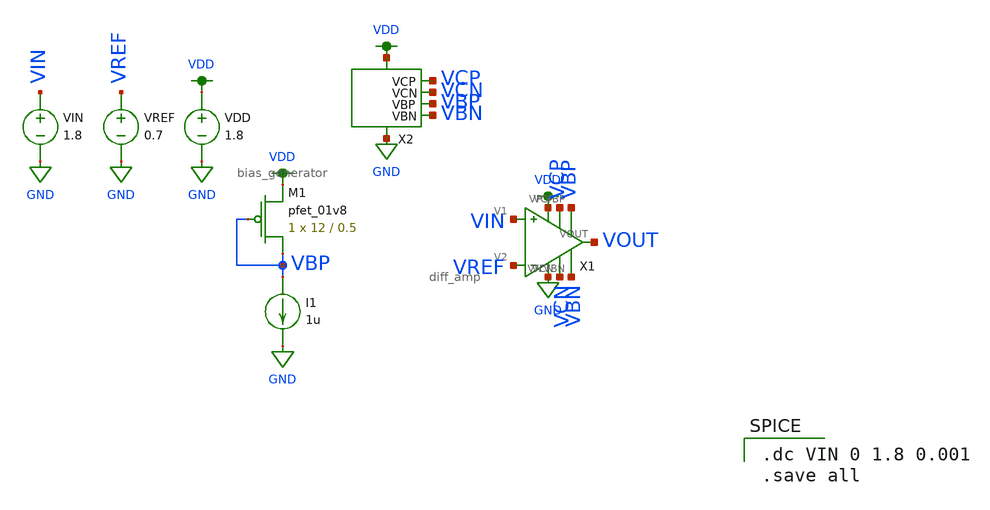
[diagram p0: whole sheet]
** sch_path: mp3/schematics/bias_generator_tran.sch
**.subckt bias_generator_tran
VDD VDD GND 1.8
I1 VBP GND 1u
VREF VREF GND 0.7
VIN VIN GND 1.8
XM1 VBP VBP VDD VDD sky130_fd_pr__pfet_01v8 L=0.5 W=12 nf=1 ad='int((nf+1)/2) * W/nf * 0.29' as='int((nf+2)/2) * W/nf * 0.29'
+ pd='2*int((nf+1)/2) * (W/nf + 0.29)' ps='2*int((nf+2)/2) * (W/nf + 0.29)' nrd='0.29 / W' nrs='0.29 / W'
+ sa=0 sb=0 sd=0 mult=1 m=1
X1 VIN VREF VDD GND VCN VBN VBP VCP VOUT diff_amp
X2 VDD GND VCN VCP VBP VBN bias_generator
**** begin user architecture code

.option wnflag=1
.lib ~/skywater/skywater-pdk/libraries/sky130_fd_pr_ngspice/latest/models/sky130.lib.spice tt


.dc VIN 0 1.8 0.001
.save all

**** end user architecture code
**.ends

* expanding   symbol:  /home/madvlsi/Documents/VLSI/mp3/schematics/diff_amp.sym # of pins=9
** sym_path: mp3/schematics/diff_amp.sym
** sch_path: mp3/schematics/diff_amp.sch
.subckt diff_amp V1 V2 VP VN VCN VBN VBP VCP VOUT
*.ipin V1
*.ipin V2
*.iopin VP
*.iopin VN
*.opin VOUT
*.iopin VBP
*.iopin VCP
*.iopin VCN
*.iopin VBN
XM1 net1 VBP VP VP sky130_fd_pr__pfet_01v8 L=0.5 W=12 nf=1 ad='int((nf+1)/2) * W/nf * 0.29' as='int((nf+2)/2) * W/nf * 0.29'
+ pd='2*int((nf+1)/2) * (W/nf + 0.29)' ps='2*int((nf+2)/2) * (W/nf + 0.29)' nrd='0.29 / W' nrs='0.29 / W'
+ sa=0 sb=0 sd=0 mult=1 m=1
XM5 net3 VCN net4 VN sky130_fd_pr__nfet_01v8 L=0.5 W=12 nf=1 ad='int((nf+1)/2) * W/nf * 0.29' as='int((nf+2)/2) * W/nf * 0.29'
+ pd='2*int((nf+1)/2) * (W/nf + 0.29)' ps='2*int((nf+2)/2) * (W/nf + 0.29)' nrd='0.29 / W' nrs='0.29 / W'
+ sa=0 sb=0 sd=0 mult=1 m=1
XM2 net2 VBP VP VP sky130_fd_pr__pfet_01v8 L=0.5 W=12 nf=1 ad='int((nf+1)/2) * W/nf * 0.29' as='int((nf+2)/2) * W/nf * 0.29'
+ pd='2*int((nf+1)/2) * (W/nf + 0.29)' ps='2*int((nf+2)/2) * (W/nf + 0.29)' nrd='0.29 / W' nrs='0.29 / W'
+ sa=0 sb=0 sd=0 mult=1 m=1
XM3 VOUT VCP net2 VP sky130_fd_pr__pfet_01v8 L=0.5 W=12 nf=1 ad='int((nf+1)/2) * W/nf * 0.29' as='int((nf+2)/2) * W/nf * 0.29'
+ pd='2*int((nf+1)/2) * (W/nf + 0.29)' ps='2*int((nf+2)/2) * (W/nf + 0.29)' nrd='0.29 / W' nrs='0.29 / W'
+ sa=0 sb=0 sd=0 mult=1 m=1
XM4 net3 VCP net1 VP sky130_fd_pr__pfet_01v8 L=0.5 W=12 nf=1 ad='int((nf+1)/2) * W/nf * 0.29' as='int((nf+2)/2) * W/nf * 0.29'
+ pd='2*int((nf+1)/2) * (W/nf + 0.29)' ps='2*int((nf+2)/2) * (W/nf + 0.29)' nrd='0.29 / W' nrs='0.29 / W'
+ sa=0 sb=0 sd=0 mult=1 m=1
XM6 net1 V1 net6 VN sky130_fd_pr__nfet_01v8 L=0.5 W=12 nf=1 ad='int((nf+1)/2) * W/nf * 0.29' as='int((nf+2)/2) * W/nf * 0.29'
+ pd='2*int((nf+1)/2) * (W/nf + 0.29)' ps='2*int((nf+2)/2) * (W/nf + 0.29)' nrd='0.29 / W' nrs='0.29 / W'
+ sa=0 sb=0 sd=0 mult=1 m=1
XM7 net2 V2 net6 VN sky130_fd_pr__nfet_01v8 L=0.5 W=12 nf=1 ad='int((nf+1)/2) * W/nf * 0.29' as='int((nf+2)/2) * W/nf * 0.29'
+ pd='2*int((nf+1)/2) * (W/nf + 0.29)' ps='2*int((nf+2)/2) * (W/nf + 0.29)' nrd='0.29 / W' nrs='0.29 / W'
+ sa=0 sb=0 sd=0 mult=1 m=1
XM8 VOUT VCN net5 VN sky130_fd_pr__nfet_01v8 L=0.5 W=12 nf=1 ad='int((nf+1)/2) * W/nf * 0.29' as='int((nf+2)/2) * W/nf * 0.29'
+ pd='2*int((nf+1)/2) * (W/nf + 0.29)' ps='2*int((nf+2)/2) * (W/nf + 0.29)' nrd='0.29 / W' nrs='0.29 / W'
+ sa=0 sb=0 sd=0 mult=1 m=1
XM9 net5 net3 VN VN sky130_fd_pr__nfet_01v8 L=0.5 W=12 nf=1 ad='int((nf+1)/2) * W/nf * 0.29' as='int((nf+2)/2) * W/nf * 0.29'
+ pd='2*int((nf+1)/2) * (W/nf + 0.29)' ps='2*int((nf+2)/2) * (W/nf + 0.29)' nrd='0.29 / W' nrs='0.29 / W'
+ sa=0 sb=0 sd=0 mult=1 m=1
XM10 net4 net3 VN VN sky130_fd_pr__nfet_01v8 L=0.5 W=12 nf=1 ad='int((nf+1)/2) * W/nf * 0.29' as='int((nf+2)/2) * W/nf * 0.29'
+ pd='2*int((nf+1)/2) * (W/nf + 0.29)' ps='2*int((nf+2)/2) * (W/nf + 0.29)' nrd='0.29 / W' nrs='0.29 / W'
+ sa=0 sb=0 sd=0 mult=1 m=1
XM11 net6 VBN VN VN sky130_fd_pr__nfet_01v8 L=0.5 W=12 nf=1 ad='int((nf+1)/2) * W/nf * 0.29' as='int((nf+2)/2) * W/nf * 0.29'
+ pd='2*int((nf+1)/2) * (W/nf + 0.29)' ps='2*int((nf+2)/2) * (W/nf + 0.29)' nrd='0.29 / W' nrs='0.29 / W'
+ sa=0 sb=0 sd=0 mult=1 m=1
.ends


* expanding   symbol:  /home/madvlsi/Documents/VLSI/mp3/schematics/bias_generator.sym # of pins=6
** sym_path: mp3/schematics/bias_generator.sym
** sch_path: mp3/schematics/bias_generator.sch
.subckt bias_generator VP VN VCN VCP VBP VBN
*.iopin VBP
*.iopin VP
*.iopin VN
*.opin VCN
*.opin VCP
*.opin VBN
XM9 VCN VP VP VP sky130_fd_pr__pfet_01v8 L=0.5 W=12 nf=1 ad='int((nf+1)/2) * W/nf * 0.29' as='int((nf+2)/2) * W/nf * 0.29'
+ pd='2*int((nf+1)/2) * (W/nf + 0.29)' ps='2*int((nf+2)/2) * (W/nf + 0.29)' nrd='0.29 / W' nrs='0.29 / W'
+ sa=0 sb=0 sd=0 mult=1 m=1
XM24 VCN VCN net10 GND sky130_fd_pr__nfet_01v8 L=0.5 W=12 nf=1 ad='int((nf+1)/2) * W/nf * 0.29' as='int((nf+2)/2) * W/nf * 0.29'
+ pd='2*int((nf+1)/2) * (W/nf + 0.29)' ps='2*int((nf+2)/2) * (W/nf + 0.29)' nrd='0.29 / W' nrs='0.29 / W'
+ sa=0 sb=0 sd=0 mult=1 m=1
XM2 VCN VBP VP VDD sky130_fd_pr__pfet_01v8 L=0.5 W=12 nf=1 ad='int((nf+1)/2) * W/nf * 0.29' as='int((nf+2)/2) * W/nf * 0.29'
+ pd='2*int((nf+1)/2) * (W/nf + 0.29)' ps='2*int((nf+2)/2) * (W/nf + 0.29)' nrd='0.29 / W' nrs='0.29 / W'
+ sa=0 sb=0 sd=0 mult=1 m=1
XM1 VP VBP net1 VDD sky130_fd_pr__pfet_01v8 L=0.5 W=12 nf=1 ad='int((nf+1)/2) * W/nf * 0.29' as='int((nf+2)/2) * W/nf * 0.29'
+ pd='2*int((nf+1)/2) * (W/nf + 0.29)' ps='2*int((nf+2)/2) * (W/nf + 0.29)' nrd='0.29 / W' nrs='0.29 / W'
+ sa=0 sb=0 sd=0 mult=1 m=1
XM3 net1 VBP net2 VDD sky130_fd_pr__pfet_01v8 L=0.5 W=12 nf=1 ad='int((nf+1)/2) * W/nf * 0.29' as='int((nf+2)/2) * W/nf * 0.29'
+ pd='2*int((nf+1)/2) * (W/nf + 0.29)' ps='2*int((nf+2)/2) * (W/nf + 0.29)' nrd='0.29 / W' nrs='0.29 / W'
+ sa=0 sb=0 sd=0 mult=1 m=1
XM4 net2 VBP net3 VDD sky130_fd_pr__pfet_01v8 L=0.5 W=12 nf=1 ad='int((nf+1)/2) * W/nf * 0.29' as='int((nf+2)/2) * W/nf * 0.29'
+ pd='2*int((nf+1)/2) * (W/nf + 0.29)' ps='2*int((nf+2)/2) * (W/nf + 0.29)' nrd='0.29 / W' nrs='0.29 / W'
+ sa=0 sb=0 sd=0 mult=1 m=1
XM6 net3 VBP net4 VDD sky130_fd_pr__pfet_01v8 L=0.5 W=12 nf=1 ad='int((nf+1)/2) * W/nf * 0.29' as='int((nf+2)/2) * W/nf * 0.29'
+ pd='2*int((nf+1)/2) * (W/nf + 0.29)' ps='2*int((nf+2)/2) * (W/nf + 0.29)' nrd='0.29 / W' nrs='0.29 / W'
+ sa=0 sb=0 sd=0 mult=1 m=1
XM7 net4 VBP net9 VDD sky130_fd_pr__pfet_01v8 L=0.5 W=12 nf=1 ad='int((nf+1)/2) * W/nf * 0.29' as='int((nf+2)/2) * W/nf * 0.29'
+ pd='2*int((nf+1)/2) * (W/nf + 0.29)' ps='2*int((nf+2)/2) * (W/nf + 0.29)' nrd='0.29 / W' nrs='0.29 / W'
+ sa=0 sb=0 sd=0 mult=1 m=1
XM8 net9 VBP net5 VDD sky130_fd_pr__pfet_01v8 L=0.5 W=12 nf=1 ad='int((nf+1)/2) * W/nf * 0.29' as='int((nf+2)/2) * W/nf * 0.29'
+ pd='2*int((nf+1)/2) * (W/nf + 0.29)' ps='2*int((nf+2)/2) * (W/nf + 0.29)' nrd='0.29 / W' nrs='0.29 / W'
+ sa=0 sb=0 sd=0 mult=1 m=1
XM52 net5 VBP net6 VDD sky130_fd_pr__pfet_01v8 L=0.5 W=12 nf=1 ad='int((nf+1)/2) * W/nf * 0.29' as='int((nf+2)/2) * W/nf * 0.29'
+ pd='2*int((nf+1)/2) * (W/nf + 0.29)' ps='2*int((nf+2)/2) * (W/nf + 0.29)' nrd='0.29 / W' nrs='0.29 / W'
+ sa=0 sb=0 sd=0 mult=1 m=1
XM53 net6 VBP net7 VDD sky130_fd_pr__pfet_01v8 L=0.5 W=12 nf=1 ad='int((nf+1)/2) * W/nf * 0.29' as='int((nf+2)/2) * W/nf * 0.29'
+ pd='2*int((nf+1)/2) * (W/nf + 0.29)' ps='2*int((nf+2)/2) * (W/nf + 0.29)' nrd='0.29 / W' nrs='0.29 / W'
+ sa=0 sb=0 sd=0 mult=1 m=1
XM54 net7 VBP net8 VDD sky130_fd_pr__pfet_01v8 L=0.5 W=12 nf=1 ad='int((nf+1)/2) * W/nf * 0.29' as='int((nf+2)/2) * W/nf * 0.29'
+ pd='2*int((nf+1)/2) * (W/nf + 0.29)' ps='2*int((nf+2)/2) * (W/nf + 0.29)' nrd='0.29 / W' nrs='0.29 / W'
+ sa=0 sb=0 sd=0 mult=1 m=1
XM55 net8 VBP VP VDD sky130_fd_pr__pfet_01v8 L=0.5 W=12 nf=1 ad='int((nf+1)/2) * W/nf * 0.29' as='int((nf+2)/2) * W/nf * 0.29'
+ pd='2*int((nf+1)/2) * (W/nf + 0.29)' ps='2*int((nf+2)/2) * (W/nf + 0.29)' nrd='0.29 / W' nrs='0.29 / W'
+ sa=0 sb=0 sd=0 mult=1 m=1
XM56 VP VBP VCN VDD sky130_fd_pr__pfet_01v8 L=0.5 W=12 nf=1 ad='int((nf+1)/2) * W/nf * 0.29' as='int((nf+2)/2) * W/nf * 0.29'
+ pd='2*int((nf+1)/2) * (W/nf + 0.29)' ps='2*int((nf+2)/2) * (W/nf + 0.29)' nrd='0.29 / W' nrs='0.29 / W'
+ sa=0 sb=0 sd=0 mult=1 m=1
XM10 VP VP VCN VP sky130_fd_pr__pfet_01v8 L=0.5 W=12 nf=1 ad='int((nf+1)/2) * W/nf * 0.29' as='int((nf+2)/2) * W/nf * 0.29'
+ pd='2*int((nf+1)/2) * (W/nf + 0.29)' ps='2*int((nf+2)/2) * (W/nf + 0.29)' nrd='0.29 / W' nrs='0.29 / W'
+ sa=0 sb=0 sd=0 mult=1 m=1
XM25 VN VN VCN VN sky130_fd_pr__nfet_01v8 L=0.5 W=12 nf=1 ad='int((nf+1)/2) * W/nf * 0.29' as='int((nf+2)/2) * W/nf * 0.29'
+ pd='2*int((nf+1)/2) * (W/nf + 0.29)' ps='2*int((nf+2)/2) * (W/nf + 0.29)' nrd='0.29 / W' nrs='0.29 / W'
+ sa=0 sb=0 sd=0 mult=1 m=1
XM14 net9 net9 net10 GND sky130_fd_pr__nfet_01v8 L=0.5 W=12 nf=1 ad='int((nf+1)/2) * W/nf * 0.29' as='int((nf+2)/2) * W/nf * 0.29'
+ pd='2*int((nf+1)/2) * (W/nf + 0.29)' ps='2*int((nf+2)/2) * (W/nf + 0.29)' nrd='0.29 / W' nrs='0.29 / W'
+ sa=0 sb=0 sd=0 mult=1 m=1
XM15 net10 net9 net9 GND sky130_fd_pr__nfet_01v8 L=0.5 W=12 nf=1 ad='int((nf+1)/2) * W/nf * 0.29' as='int((nf+2)/2) * W/nf * 0.29'
+ pd='2*int((nf+1)/2) * (W/nf + 0.29)' ps='2*int((nf+2)/2) * (W/nf + 0.29)' nrd='0.29 / W' nrs='0.29 / W'
+ sa=0 sb=0 sd=0 mult=1 m=1
XM16 net9 net9 net10 GND sky130_fd_pr__nfet_01v8 L=0.5 W=12 nf=1 ad='int((nf+1)/2) * W/nf * 0.29' as='int((nf+2)/2) * W/nf * 0.29'
+ pd='2*int((nf+1)/2) * (W/nf + 0.29)' ps='2*int((nf+2)/2) * (W/nf + 0.29)' nrd='0.29 / W' nrs='0.29 / W'
+ sa=0 sb=0 sd=0 mult=1 m=1
XM17 net10 net9 net9 GND sky130_fd_pr__nfet_01v8 L=0.5 W=12 nf=1 ad='int((nf+1)/2) * W/nf * 0.29' as='int((nf+2)/2) * W/nf * 0.29'
+ pd='2*int((nf+1)/2) * (W/nf + 0.29)' ps='2*int((nf+2)/2) * (W/nf + 0.29)' nrd='0.29 / W' nrs='0.29 / W'
+ sa=0 sb=0 sd=0 mult=1 m=1
XM18 VN net9 net10 GND sky130_fd_pr__nfet_01v8 L=0.5 W=12 nf=1 ad='int((nf+1)/2) * W/nf * 0.29' as='int((nf+2)/2) * W/nf * 0.29'
+ pd='2*int((nf+1)/2) * (W/nf + 0.29)' ps='2*int((nf+2)/2) * (W/nf + 0.29)' nrd='0.29 / W' nrs='0.29 / W'
+ sa=0 sb=0 sd=0 mult=1 m=1
XM19 net10 net9 VN GND sky130_fd_pr__nfet_01v8 L=0.5 W=12 nf=1 ad='int((nf+1)/2) * W/nf * 0.29' as='int((nf+2)/2) * W/nf * 0.29'
+ pd='2*int((nf+1)/2) * (W/nf + 0.29)' ps='2*int((nf+2)/2) * (W/nf + 0.29)' nrd='0.29 / W' nrs='0.29 / W'
+ sa=0 sb=0 sd=0 mult=1 m=1
XM20 net9 net9 net10 GND sky130_fd_pr__nfet_01v8 L=0.5 W=12 nf=1 ad='int((nf+1)/2) * W/nf * 0.29' as='int((nf+2)/2) * W/nf * 0.29'
+ pd='2*int((nf+1)/2) * (W/nf + 0.29)' ps='2*int((nf+2)/2) * (W/nf + 0.29)' nrd='0.29 / W' nrs='0.29 / W'
+ sa=0 sb=0 sd=0 mult=1 m=1
XM21 net10 net9 net9 GND sky130_fd_pr__nfet_01v8 L=0.5 W=12 nf=1 ad='int((nf+1)/2) * W/nf * 0.29' as='int((nf+2)/2) * W/nf * 0.29'
+ pd='2*int((nf+1)/2) * (W/nf + 0.29)' ps='2*int((nf+2)/2) * (W/nf + 0.29)' nrd='0.29 / W' nrs='0.29 / W'
+ sa=0 sb=0 sd=0 mult=1 m=1
XM22 net9 net9 net10 GND sky130_fd_pr__nfet_01v8 L=0.5 W=12 nf=1 ad='int((nf+1)/2) * W/nf * 0.29' as='int((nf+2)/2) * W/nf * 0.29'
+ pd='2*int((nf+1)/2) * (W/nf + 0.29)' ps='2*int((nf+2)/2) * (W/nf + 0.29)' nrd='0.29 / W' nrs='0.29 / W'
+ sa=0 sb=0 sd=0 mult=1 m=1
XM23 net10 net9 net9 GND sky130_fd_pr__nfet_01v8 L=0.5 W=12 nf=1 ad='int((nf+1)/2) * W/nf * 0.29' as='int((nf+2)/2) * W/nf * 0.29'
+ pd='2*int((nf+1)/2) * (W/nf + 0.29)' ps='2*int((nf+2)/2) * (W/nf + 0.29)' nrd='0.29 / W' nrs='0.29 / W'
+ sa=0 sb=0 sd=0 mult=1 m=1
XM5 net10 VCN VCN GND sky130_fd_pr__nfet_01v8 L=0.5 W=12 nf=1 ad='int((nf+1)/2) * W/nf * 0.29' as='int((nf+2)/2) * W/nf * 0.29'
+ pd='2*int((nf+1)/2) * (W/nf + 0.29)' ps='2*int((nf+2)/2) * (W/nf + 0.29)' nrd='0.29 / W' nrs='0.29 / W'
+ sa=0 sb=0 sd=0 mult=1 m=1
XM26 VCN VN VN VN sky130_fd_pr__nfet_01v8 L=0.5 W=12 nf=1 ad='int((nf+1)/2) * W/nf * 0.29' as='int((nf+2)/2) * W/nf * 0.29'
+ pd='2*int((nf+1)/2) * (W/nf + 0.29)' ps='2*int((nf+2)/2) * (W/nf + 0.29)' nrd='0.29 / W' nrs='0.29 / W'
+ sa=0 sb=0 sd=0 mult=1 m=1
XM27 net13 VBN VN GND sky130_fd_pr__nfet_01v8 L=0.5 W=12 nf=1 ad='int((nf+1)/2) * W/nf * 0.29' as='int((nf+2)/2) * W/nf * 0.29'
+ pd='2*int((nf+1)/2) * (W/nf + 0.29)' ps='2*int((nf+2)/2) * (W/nf + 0.29)' nrd='0.29 / W' nrs='0.29 / W'
+ sa=0 sb=0 sd=0 mult=1 m=1
XM39 net14 VBN net13 GND sky130_fd_pr__nfet_01v8 L=0.5 W=12 nf=1 ad='int((nf+1)/2) * W/nf * 0.29' as='int((nf+2)/2) * W/nf * 0.29'
+ pd='2*int((nf+1)/2) * (W/nf + 0.29)' ps='2*int((nf+2)/2) * (W/nf + 0.29)' nrd='0.29 / W' nrs='0.29 / W'
+ sa=0 sb=0 sd=0 mult=1 m=1
XM40 net15 VBN net14 GND sky130_fd_pr__nfet_01v8 L=0.5 W=12 nf=1 ad='int((nf+1)/2) * W/nf * 0.29' as='int((nf+2)/2) * W/nf * 0.29'
+ pd='2*int((nf+1)/2) * (W/nf + 0.29)' ps='2*int((nf+2)/2) * (W/nf + 0.29)' nrd='0.29 / W' nrs='0.29 / W'
+ sa=0 sb=0 sd=0 mult=1 m=1
XM41 net16 VBN net15 GND sky130_fd_pr__nfet_01v8 L=0.5 W=12 nf=1 ad='int((nf+1)/2) * W/nf * 0.29' as='int((nf+2)/2) * W/nf * 0.29'
+ pd='2*int((nf+1)/2) * (W/nf + 0.29)' ps='2*int((nf+2)/2) * (W/nf + 0.29)' nrd='0.29 / W' nrs='0.29 / W'
+ sa=0 sb=0 sd=0 mult=1 m=1
XM42 net11 VBN net16 GND sky130_fd_pr__nfet_01v8 L=0.5 W=12 nf=1 ad='int((nf+1)/2) * W/nf * 0.29' as='int((nf+2)/2) * W/nf * 0.29'
+ pd='2*int((nf+1)/2) * (W/nf + 0.29)' ps='2*int((nf+2)/2) * (W/nf + 0.29)' nrd='0.29 / W' nrs='0.29 / W'
+ sa=0 sb=0 sd=0 mult=1 m=1
XM43 net17 VBN net11 GND sky130_fd_pr__nfet_01v8 L=0.5 W=12 nf=1 ad='int((nf+1)/2) * W/nf * 0.29' as='int((nf+2)/2) * W/nf * 0.29'
+ pd='2*int((nf+1)/2) * (W/nf + 0.29)' ps='2*int((nf+2)/2) * (W/nf + 0.29)' nrd='0.29 / W' nrs='0.29 / W'
+ sa=0 sb=0 sd=0 mult=1 m=1
XM44 net18 VBN net17 GND sky130_fd_pr__nfet_01v8 L=0.5 W=12 nf=1 ad='int((nf+1)/2) * W/nf * 0.29' as='int((nf+2)/2) * W/nf * 0.29'
+ pd='2*int((nf+1)/2) * (W/nf + 0.29)' ps='2*int((nf+2)/2) * (W/nf + 0.29)' nrd='0.29 / W' nrs='0.29 / W'
+ sa=0 sb=0 sd=0 mult=1 m=1
XM45 net19 VBN net18 GND sky130_fd_pr__nfet_01v8 L=0.5 W=12 nf=1 ad='int((nf+1)/2) * W/nf * 0.29' as='int((nf+2)/2) * W/nf * 0.29'
+ pd='2*int((nf+1)/2) * (W/nf + 0.29)' ps='2*int((nf+2)/2) * (W/nf + 0.29)' nrd='0.29 / W' nrs='0.29 / W'
+ sa=0 sb=0 sd=0 mult=1 m=1
XM46 net20 VBN net19 GND sky130_fd_pr__nfet_01v8 L=0.5 W=12 nf=1 ad='int((nf+1)/2) * W/nf * 0.29' as='int((nf+2)/2) * W/nf * 0.29'
+ pd='2*int((nf+1)/2) * (W/nf + 0.29)' ps='2*int((nf+2)/2) * (W/nf + 0.29)' nrd='0.29 / W' nrs='0.29 / W'
+ sa=0 sb=0 sd=0 mult=1 m=1
XM47 VN VBN net20 GND sky130_fd_pr__nfet_01v8 L=0.5 W=12 nf=1 ad='int((nf+1)/2) * W/nf * 0.29' as='int((nf+2)/2) * W/nf * 0.29'
+ pd='2*int((nf+1)/2) * (W/nf + 0.29)' ps='2*int((nf+2)/2) * (W/nf + 0.29)' nrd='0.29 / W' nrs='0.29 / W'
+ sa=0 sb=0 sd=0 mult=1 m=1
XM48 VN VBN VCP GND sky130_fd_pr__nfet_01v8 L=0.5 W=12 nf=1 ad='int((nf+1)/2) * W/nf * 0.29' as='int((nf+2)/2) * W/nf * 0.29'
+ pd='2*int((nf+1)/2) * (W/nf + 0.29)' ps='2*int((nf+2)/2) * (W/nf + 0.29)' nrd='0.29 / W' nrs='0.29 / W'
+ sa=0 sb=0 sd=0 mult=1 m=1
XM49 VCP VBN VN GND sky130_fd_pr__nfet_01v8 L=0.5 W=12 nf=1 ad='int((nf+1)/2) * W/nf * 0.29' as='int((nf+2)/2) * W/nf * 0.29'
+ pd='2*int((nf+1)/2) * (W/nf + 0.29)' ps='2*int((nf+2)/2) * (W/nf + 0.29)' nrd='0.29 / W' nrs='0.29 / W'
+ sa=0 sb=0 sd=0 mult=1 m=1
XM29 net12 net11 net11 VDD sky130_fd_pr__pfet_01v8 L=0.5 W=12 nf=1 ad='int((nf+1)/2) * W/nf * 0.29' as='int((nf+2)/2) * W/nf * 0.29'
+ pd='2*int((nf+1)/2) * (W/nf + 0.29)' ps='2*int((nf+2)/2) * (W/nf + 0.29)' nrd='0.29 / W' nrs='0.29 / W'
+ sa=0 sb=0 sd=0 mult=1 m=1
XM30 net11 net11 net12 VDD sky130_fd_pr__pfet_01v8 L=0.5 W=12 nf=1 ad='int((nf+1)/2) * W/nf * 0.29' as='int((nf+2)/2) * W/nf * 0.29'
+ pd='2*int((nf+1)/2) * (W/nf + 0.29)' ps='2*int((nf+2)/2) * (W/nf + 0.29)' nrd='0.29 / W' nrs='0.29 / W'
+ sa=0 sb=0 sd=0 mult=1 m=1
XM31 net12 net11 net11 VDD sky130_fd_pr__pfet_01v8 L=0.5 W=12 nf=1 ad='int((nf+1)/2) * W/nf * 0.29' as='int((nf+2)/2) * W/nf * 0.29'
+ pd='2*int((nf+1)/2) * (W/nf + 0.29)' ps='2*int((nf+2)/2) * (W/nf + 0.29)' nrd='0.29 / W' nrs='0.29 / W'
+ sa=0 sb=0 sd=0 mult=1 m=1
XM32 net11 net11 net12 VDD sky130_fd_pr__pfet_01v8 L=0.5 W=12 nf=1 ad='int((nf+1)/2) * W/nf * 0.29' as='int((nf+2)/2) * W/nf * 0.29'
+ pd='2*int((nf+1)/2) * (W/nf + 0.29)' ps='2*int((nf+2)/2) * (W/nf + 0.29)' nrd='0.29 / W' nrs='0.29 / W'
+ sa=0 sb=0 sd=0 mult=1 m=1
XM33 net12 net11 VP VDD sky130_fd_pr__pfet_01v8 L=0.5 W=12 nf=1 ad='int((nf+1)/2) * W/nf * 0.29' as='int((nf+2)/2) * W/nf * 0.29'
+ pd='2*int((nf+1)/2) * (W/nf + 0.29)' ps='2*int((nf+2)/2) * (W/nf + 0.29)' nrd='0.29 / W' nrs='0.29 / W'
+ sa=0 sb=0 sd=0 mult=1 m=1
XM34 VP net11 net12 VDD sky130_fd_pr__pfet_01v8 L=0.5 W=12 nf=1 ad='int((nf+1)/2) * W/nf * 0.29' as='int((nf+2)/2) * W/nf * 0.29'
+ pd='2*int((nf+1)/2) * (W/nf + 0.29)' ps='2*int((nf+2)/2) * (W/nf + 0.29)' nrd='0.29 / W' nrs='0.29 / W'
+ sa=0 sb=0 sd=0 mult=1 m=1
XM35 net12 net11 net11 VDD sky130_fd_pr__pfet_01v8 L=0.5 W=12 nf=1 ad='int((nf+1)/2) * W/nf * 0.29' as='int((nf+2)/2) * W/nf * 0.29'
+ pd='2*int((nf+1)/2) * (W/nf + 0.29)' ps='2*int((nf+2)/2) * (W/nf + 0.29)' nrd='0.29 / W' nrs='0.29 / W'
+ sa=0 sb=0 sd=0 mult=1 m=1
XM36 net11 net11 net12 VDD sky130_fd_pr__pfet_01v8 L=0.5 W=12 nf=1 ad='int((nf+1)/2) * W/nf * 0.29' as='int((nf+2)/2) * W/nf * 0.29'
+ pd='2*int((nf+1)/2) * (W/nf + 0.29)' ps='2*int((nf+2)/2) * (W/nf + 0.29)' nrd='0.29 / W' nrs='0.29 / W'
+ sa=0 sb=0 sd=0 mult=1 m=1
XM37 net12 net11 net11 VDD sky130_fd_pr__pfet_01v8 L=0.5 W=12 nf=1 ad='int((nf+1)/2) * W/nf * 0.29' as='int((nf+2)/2) * W/nf * 0.29'
+ pd='2*int((nf+1)/2) * (W/nf + 0.29)' ps='2*int((nf+2)/2) * (W/nf + 0.29)' nrd='0.29 / W' nrs='0.29 / W'
+ sa=0 sb=0 sd=0 mult=1 m=1
XM38 net11 net11 net12 VDD sky130_fd_pr__pfet_01v8 L=0.5 W=12 nf=1 ad='int((nf+1)/2) * W/nf * 0.29' as='int((nf+2)/2) * W/nf * 0.29'
+ pd='2*int((nf+1)/2) * (W/nf + 0.29)' ps='2*int((nf+2)/2) * (W/nf + 0.29)' nrd='0.29 / W' nrs='0.29 / W'
+ sa=0 sb=0 sd=0 mult=1 m=1
XM57 VCP VCP net12 VDD sky130_fd_pr__pfet_01v8 L=0.5 W=12 nf=1 ad='int((nf+1)/2) * W/nf * 0.29' as='int((nf+2)/2) * W/nf * 0.29'
+ pd='2*int((nf+1)/2) * (W/nf + 0.29)' ps='2*int((nf+2)/2) * (W/nf + 0.29)' nrd='0.29 / W' nrs='0.29 / W'
+ sa=0 sb=0 sd=0 mult=1 m=1
XM28 net12 VCP VCP VDD sky130_fd_pr__pfet_01v8 L=0.5 W=12 nf=1 ad='int((nf+1)/2) * W/nf * 0.29' as='int((nf+2)/2) * W/nf * 0.29'
+ pd='2*int((nf+1)/2) * (W/nf + 0.29)' ps='2*int((nf+2)/2) * (W/nf + 0.29)' nrd='0.29 / W' nrs='0.29 / W'
+ sa=0 sb=0 sd=0 mult=1 m=1
XM50 VCP VP VP VP sky130_fd_pr__pfet_01v8 L=0.5 W=12 nf=1 ad='int((nf+1)/2) * W/nf * 0.29' as='int((nf+2)/2) * W/nf * 0.29'
+ pd='2*int((nf+1)/2) * (W/nf + 0.29)' ps='2*int((nf+2)/2) * (W/nf + 0.29)' nrd='0.29 / W' nrs='0.29 / W'
+ sa=0 sb=0 sd=0 mult=1 m=1
XM51 VP VP VCP VP sky130_fd_pr__pfet_01v8 L=0.5 W=12 nf=1 ad='int((nf+1)/2) * W/nf * 0.29' as='int((nf+2)/2) * W/nf * 0.29'
+ pd='2*int((nf+1)/2) * (W/nf + 0.29)' ps='2*int((nf+2)/2) * (W/nf + 0.29)' nrd='0.29 / W' nrs='0.29 / W'
+ sa=0 sb=0 sd=0 mult=1 m=1
XM58 VN VN VCP VN sky130_fd_pr__nfet_01v8 L=0.5 W=12 nf=1 ad='int((nf+1)/2) * W/nf * 0.29' as='int((nf+2)/2) * W/nf * 0.29'
+ pd='2*int((nf+1)/2) * (W/nf + 0.29)' ps='2*int((nf+2)/2) * (W/nf + 0.29)' nrd='0.29 / W' nrs='0.29 / W'
+ sa=0 sb=0 sd=0 mult=1 m=1
XM59 VCP VN VN VN sky130_fd_pr__nfet_01v8 L=0.5 W=12 nf=1 ad='int((nf+1)/2) * W/nf * 0.29' as='int((nf+2)/2) * W/nf * 0.29'
+ pd='2*int((nf+1)/2) * (W/nf + 0.29)' ps='2*int((nf+2)/2) * (W/nf + 0.29)' nrd='0.29 / W' nrs='0.29 / W'
+ sa=0 sb=0 sd=0 mult=1 m=1
XM3b VP VBP VBP VDD sky130_fd_pr__pfet_01v8 L=0.5 W=3 nf=1 ad='int((nf+1)/2) * W/nf * 0.29' as='int((nf+2)/2) * W/nf * 0.29'
+ pd='2*int((nf+1)/2) * (W/nf + 0.29)' ps='2*int((nf+2)/2) * (W/nf + 0.29)' nrd='0.29 / W' nrs='0.29 / W'
+ sa=0 sb=0 sd=0 mult=1 m=1
XM3a VBN VBP VP VDD sky130_fd_pr__pfet_01v8 L=0.5 W=3 nf=1 ad='int((nf+1)/2) * W/nf * 0.29' as='int((nf+2)/2) * W/nf * 0.29'
+ pd='2*int((nf+1)/2) * (W/nf + 0.29)' ps='2*int((nf+2)/2) * (W/nf + 0.29)' nrd='0.29 / W' nrs='0.29 / W'
+ sa=0 sb=0 sd=0 mult=1 m=1
XM4a VBP VBP VP VDD sky130_fd_pr__pfet_01v8 L=0.5 W=3 nf=1 ad='int((nf+1)/2) * W/nf * 0.29' as='int((nf+2)/2) * W/nf * 0.29'
+ pd='2*int((nf+1)/2) * (W/nf + 0.29)' ps='2*int((nf+2)/2) * (W/nf + 0.29)' nrd='0.29 / W' nrs='0.29 / W'
+ sa=0 sb=0 sd=0 mult=1 m=1
XM4b VP VBP VBN VDD sky130_fd_pr__pfet_01v8 L=0.5 W=3 nf=1 ad='int((nf+1)/2) * W/nf * 0.29' as='int((nf+2)/2) * W/nf * 0.29'
+ pd='2*int((nf+1)/2) * (W/nf + 0.29)' ps='2*int((nf+2)/2) * (W/nf + 0.29)' nrd='0.29 / W' nrs='0.29 / W'
+ sa=0 sb=0 sd=0 mult=1 m=1
XM3c VBN VBP VP VDD sky130_fd_pr__pfet_01v8 L=0.5 W=3 nf=1 ad='int((nf+1)/2) * W/nf * 0.29' as='int((nf+2)/2) * W/nf * 0.29'
+ pd='2*int((nf+1)/2) * (W/nf + 0.29)' ps='2*int((nf+2)/2) * (W/nf + 0.29)' nrd='0.29 / W' nrs='0.29 / W'
+ sa=0 sb=0 sd=0 mult=1 m=1
XM3d VP VBP VBP VDD sky130_fd_pr__pfet_01v8 L=0.5 W=3 nf=1 ad='int((nf+1)/2) * W/nf * 0.29' as='int((nf+2)/2) * W/nf * 0.29'
+ pd='2*int((nf+1)/2) * (W/nf + 0.29)' ps='2*int((nf+2)/2) * (W/nf + 0.29)' nrd='0.29 / W' nrs='0.29 / W'
+ sa=0 sb=0 sd=0 mult=1 m=1
XM4c VBP VBP VP VDD sky130_fd_pr__pfet_01v8 L=0.5 W=3 nf=1 ad='int((nf+1)/2) * W/nf * 0.29' as='int((nf+2)/2) * W/nf * 0.29'
+ pd='2*int((nf+1)/2) * (W/nf + 0.29)' ps='2*int((nf+2)/2) * (W/nf + 0.29)' nrd='0.29 / W' nrs='0.29 / W'
+ sa=0 sb=0 sd=0 mult=1 m=1
XM1e VP VP VBN VP sky130_fd_pr__pfet_01v8 L=0.5 W=3 nf=1 ad='int((nf+1)/2) * W/nf * 0.29' as='int((nf+2)/2) * W/nf * 0.29'
+ pd='2*int((nf+1)/2) * (W/nf + 0.29)' ps='2*int((nf+2)/2) * (W/nf + 0.29)' nrd='0.29 / W' nrs='0.29 / W'
+ sa=0 sb=0 sd=0 mult=1 m=1
XM1f VBN VP VP VP sky130_fd_pr__pfet_01v8 L=0.5 W=3 nf=1 ad='int((nf+1)/2) * W/nf * 0.29' as='int((nf+2)/2) * W/nf * 0.29'
+ pd='2*int((nf+1)/2) * (W/nf + 0.29)' ps='2*int((nf+2)/2) * (W/nf + 0.29)' nrd='0.29 / W' nrs='0.29 / W'
+ sa=0 sb=0 sd=0 mult=1 m=1
XM4d VP VBP VBN VDD sky130_fd_pr__pfet_01v8 L=0.5 W=3 nf=1 ad='int((nf+1)/2) * W/nf * 0.29' as='int((nf+2)/2) * W/nf * 0.29'
+ pd='2*int((nf+1)/2) * (W/nf + 0.29)' ps='2*int((nf+2)/2) * (W/nf + 0.29)' nrd='0.29 / W' nrs='0.29 / W'
+ sa=0 sb=0 sd=0 mult=1 m=1
XM60 VBN VBN VN GND sky130_fd_pr__nfet_01v8 L=0.5 W=12 nf=1 ad='int((nf+1)/2) * W/nf * 0.29' as='int((nf+2)/2) * W/nf * 0.29'
+ pd='2*int((nf+1)/2) * (W/nf + 0.29)' ps='2*int((nf+2)/2) * (W/nf + 0.29)' nrd='0.29 / W' nrs='0.29 / W'
+ sa=0 sb=0 sd=0 mult=1 m=1
.ends

.GLOBAL GND
.GLOBAL VDD
.end
